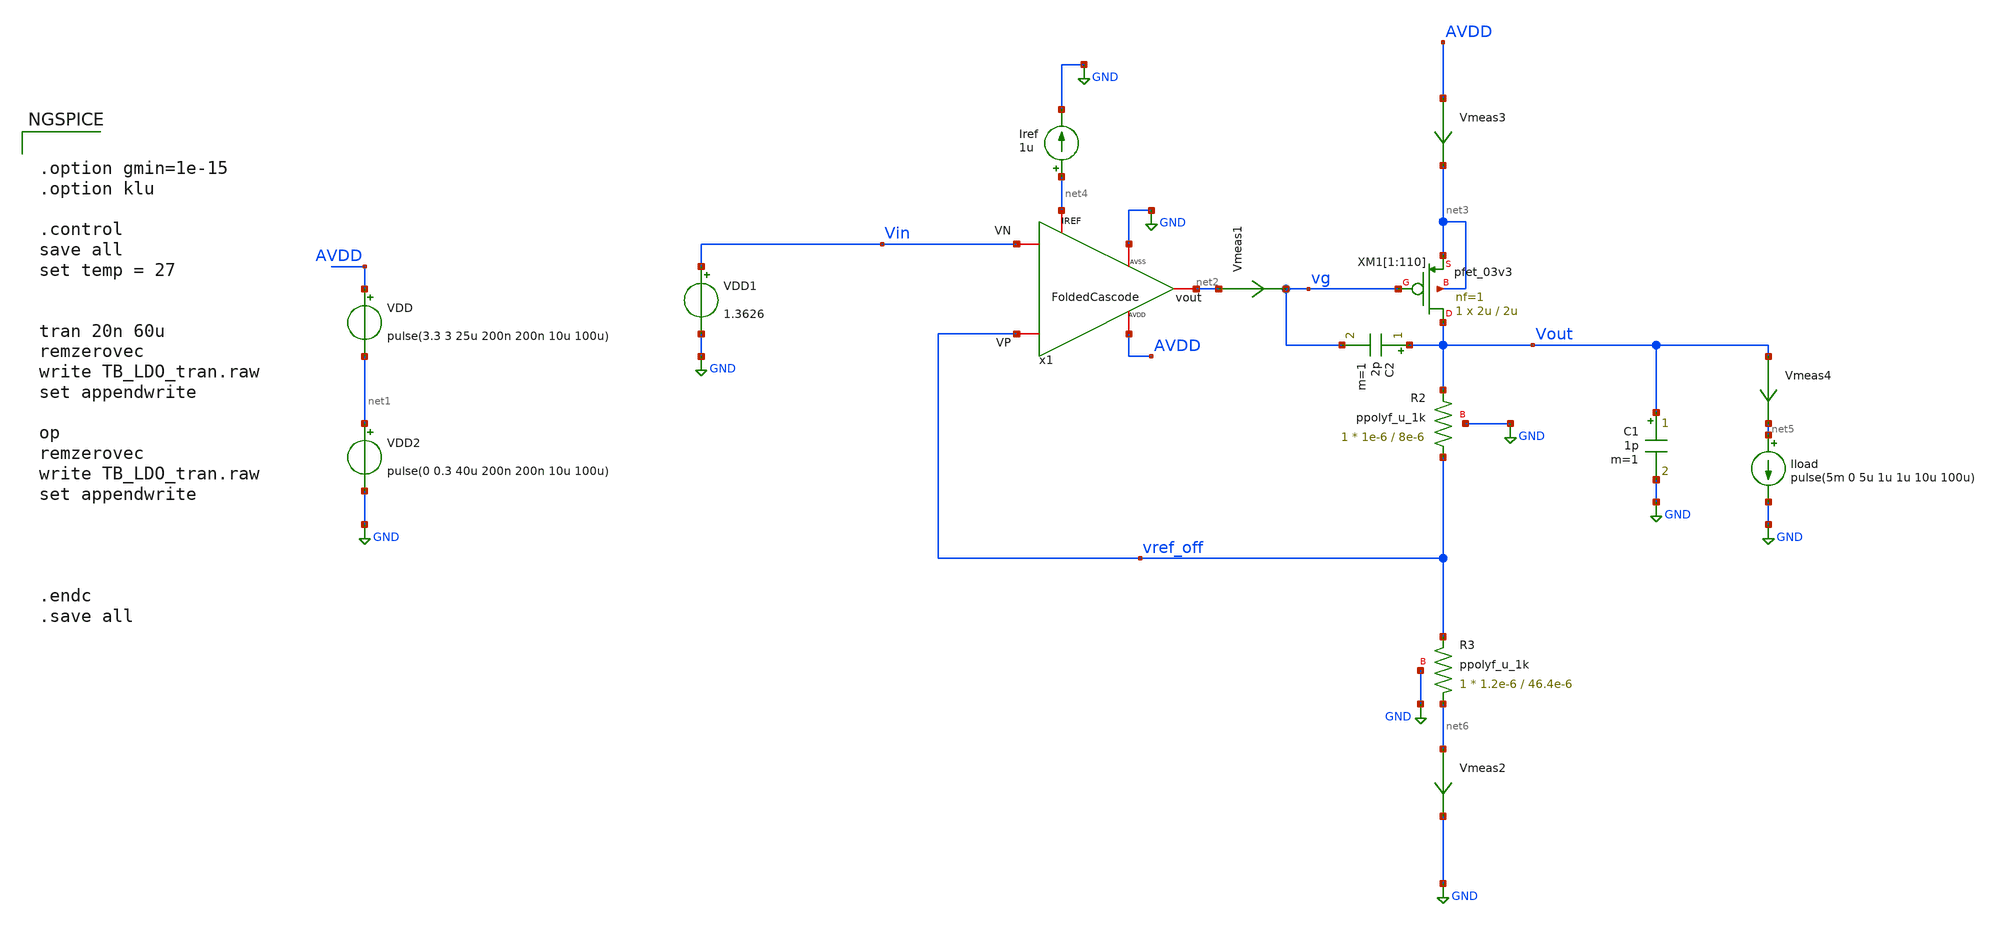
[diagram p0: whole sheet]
** sch_path: Voltage_Reference/LDO/TB_LDO_tran.sch
**.subckt TB_LDO_tran
VDD AVDD net1 pulse(3.3 3 25u 200n 200n 10u 100u)
Iref net4 GND 1u
Vmeas2 net6 GND 0
.save i(vmeas2)
XM1[1] Vout vg net3 net3 pfet_03v3 L=2u W=2u nf=1 ad='int((nf+1)/2) * W/nf * 0.18u' as='int((nf+2)/2) * W/nf * 0.18u'
+ pd='2*int((nf+1)/2) * (W/nf + 0.18u)' ps='2*int((nf+2)/2) * (W/nf + 0.18u)' nrd='0.18u / W' nrs='0.18u / W'
+ sa=0 sb=0 sd=0 m=1
XM1[2] Vout vg net3 net3 pfet_03v3 L=2u W=2u nf=1 ad='int((nf+1)/2) * W/nf * 0.18u' as='int((nf+2)/2) * W/nf * 0.18u'
+ pd='2*int((nf+1)/2) * (W/nf + 0.18u)' ps='2*int((nf+2)/2) * (W/nf + 0.18u)' nrd='0.18u / W' nrs='0.18u / W'
+ sa=0 sb=0 sd=0 m=1
XM1[3] Vout vg net3 net3 pfet_03v3 L=2u W=2u nf=1 ad='int((nf+1)/2) * W/nf * 0.18u' as='int((nf+2)/2) * W/nf * 0.18u'
+ pd='2*int((nf+1)/2) * (W/nf + 0.18u)' ps='2*int((nf+2)/2) * (W/nf + 0.18u)' nrd='0.18u / W' nrs='0.18u / W'
+ sa=0 sb=0 sd=0 m=1
XM1[4] Vout vg net3 net3 pfet_03v3 L=2u W=2u nf=1 ad='int((nf+1)/2) * W/nf * 0.18u' as='int((nf+2)/2) * W/nf * 0.18u'
+ pd='2*int((nf+1)/2) * (W/nf + 0.18u)' ps='2*int((nf+2)/2) * (W/nf + 0.18u)' nrd='0.18u / W' nrs='0.18u / W'
+ sa=0 sb=0 sd=0 m=1
XM1[5] Vout vg net3 net3 pfet_03v3 L=2u W=2u nf=1 ad='int((nf+1)/2) * W/nf * 0.18u' as='int((nf+2)/2) * W/nf * 0.18u'
+ pd='2*int((nf+1)/2) * (W/nf + 0.18u)' ps='2*int((nf+2)/2) * (W/nf + 0.18u)' nrd='0.18u / W' nrs='0.18u / W'
+ sa=0 sb=0 sd=0 m=1
XM1[6] Vout vg net3 net3 pfet_03v3 L=2u W=2u nf=1 ad='int((nf+1)/2) * W/nf * 0.18u' as='int((nf+2)/2) * W/nf * 0.18u'
+ pd='2*int((nf+1)/2) * (W/nf + 0.18u)' ps='2*int((nf+2)/2) * (W/nf + 0.18u)' nrd='0.18u / W' nrs='0.18u / W'
+ sa=0 sb=0 sd=0 m=1
XM1[7] Vout vg net3 net3 pfet_03v3 L=2u W=2u nf=1 ad='int((nf+1)/2) * W/nf * 0.18u' as='int((nf+2)/2) * W/nf * 0.18u'
+ pd='2*int((nf+1)/2) * (W/nf + 0.18u)' ps='2*int((nf+2)/2) * (W/nf + 0.18u)' nrd='0.18u / W' nrs='0.18u / W'
+ sa=0 sb=0 sd=0 m=1
XM1[8] Vout vg net3 net3 pfet_03v3 L=2u W=2u nf=1 ad='int((nf+1)/2) * W/nf * 0.18u' as='int((nf+2)/2) * W/nf * 0.18u'
+ pd='2*int((nf+1)/2) * (W/nf + 0.18u)' ps='2*int((nf+2)/2) * (W/nf + 0.18u)' nrd='0.18u / W' nrs='0.18u / W'
+ sa=0 sb=0 sd=0 m=1
XM1[9] Vout vg net3 net3 pfet_03v3 L=2u W=2u nf=1 ad='int((nf+1)/2) * W/nf * 0.18u' as='int((nf+2)/2) * W/nf * 0.18u'
+ pd='2*int((nf+1)/2) * (W/nf + 0.18u)' ps='2*int((nf+2)/2) * (W/nf + 0.18u)' nrd='0.18u / W' nrs='0.18u / W'
+ sa=0 sb=0 sd=0 m=1
XM1[10] Vout vg net3 net3 pfet_03v3 L=2u W=2u nf=1 ad='int((nf+1)/2) * W/nf * 0.18u' as='int((nf+2)/2) * W/nf * 0.18u'
+ pd='2*int((nf+1)/2) * (W/nf + 0.18u)' ps='2*int((nf+2)/2) * (W/nf + 0.18u)' nrd='0.18u / W' nrs='0.18u / W'
+ sa=0 sb=0 sd=0 m=1
XM1[11] Vout vg net3 net3 pfet_03v3 L=2u W=2u nf=1 ad='int((nf+1)/2) * W/nf * 0.18u' as='int((nf+2)/2) * W/nf * 0.18u'
+ pd='2*int((nf+1)/2) * (W/nf + 0.18u)' ps='2*int((nf+2)/2) * (W/nf + 0.18u)' nrd='0.18u / W' nrs='0.18u / W'
+ sa=0 sb=0 sd=0 m=1
XM1[12] Vout vg net3 net3 pfet_03v3 L=2u W=2u nf=1 ad='int((nf+1)/2) * W/nf * 0.18u' as='int((nf+2)/2) * W/nf * 0.18u'
+ pd='2*int((nf+1)/2) * (W/nf + 0.18u)' ps='2*int((nf+2)/2) * (W/nf + 0.18u)' nrd='0.18u / W' nrs='0.18u / W'
+ sa=0 sb=0 sd=0 m=1
XM1[13] Vout vg net3 net3 pfet_03v3 L=2u W=2u nf=1 ad='int((nf+1)/2) * W/nf * 0.18u' as='int((nf+2)/2) * W/nf * 0.18u'
+ pd='2*int((nf+1)/2) * (W/nf + 0.18u)' ps='2*int((nf+2)/2) * (W/nf + 0.18u)' nrd='0.18u / W' nrs='0.18u / W'
+ sa=0 sb=0 sd=0 m=1
XM1[14] Vout vg net3 net3 pfet_03v3 L=2u W=2u nf=1 ad='int((nf+1)/2) * W/nf * 0.18u' as='int((nf+2)/2) * W/nf * 0.18u'
+ pd='2*int((nf+1)/2) * (W/nf + 0.18u)' ps='2*int((nf+2)/2) * (W/nf + 0.18u)' nrd='0.18u / W' nrs='0.18u / W'
+ sa=0 sb=0 sd=0 m=1
XM1[15] Vout vg net3 net3 pfet_03v3 L=2u W=2u nf=1 ad='int((nf+1)/2) * W/nf * 0.18u' as='int((nf+2)/2) * W/nf * 0.18u'
+ pd='2*int((nf+1)/2) * (W/nf + 0.18u)' ps='2*int((nf+2)/2) * (W/nf + 0.18u)' nrd='0.18u / W' nrs='0.18u / W'
+ sa=0 sb=0 sd=0 m=1
XM1[16] Vout vg net3 net3 pfet_03v3 L=2u W=2u nf=1 ad='int((nf+1)/2) * W/nf * 0.18u' as='int((nf+2)/2) * W/nf * 0.18u'
+ pd='2*int((nf+1)/2) * (W/nf + 0.18u)' ps='2*int((nf+2)/2) * (W/nf + 0.18u)' nrd='0.18u / W' nrs='0.18u / W'
+ sa=0 sb=0 sd=0 m=1
XM1[17] Vout vg net3 net3 pfet_03v3 L=2u W=2u nf=1 ad='int((nf+1)/2) * W/nf * 0.18u' as='int((nf+2)/2) * W/nf * 0.18u'
+ pd='2*int((nf+1)/2) * (W/nf + 0.18u)' ps='2*int((nf+2)/2) * (W/nf + 0.18u)' nrd='0.18u / W' nrs='0.18u / W'
+ sa=0 sb=0 sd=0 m=1
XM1[18] Vout vg net3 net3 pfet_03v3 L=2u W=2u nf=1 ad='int((nf+1)/2) * W/nf * 0.18u' as='int((nf+2)/2) * W/nf * 0.18u'
+ pd='2*int((nf+1)/2) * (W/nf + 0.18u)' ps='2*int((nf+2)/2) * (W/nf + 0.18u)' nrd='0.18u / W' nrs='0.18u / W'
+ sa=0 sb=0 sd=0 m=1
XM1[19] Vout vg net3 net3 pfet_03v3 L=2u W=2u nf=1 ad='int((nf+1)/2) * W/nf * 0.18u' as='int((nf+2)/2) * W/nf * 0.18u'
+ pd='2*int((nf+1)/2) * (W/nf + 0.18u)' ps='2*int((nf+2)/2) * (W/nf + 0.18u)' nrd='0.18u / W' nrs='0.18u / W'
+ sa=0 sb=0 sd=0 m=1
XM1[20] Vout vg net3 net3 pfet_03v3 L=2u W=2u nf=1 ad='int((nf+1)/2) * W/nf * 0.18u' as='int((nf+2)/2) * W/nf * 0.18u'
+ pd='2*int((nf+1)/2) * (W/nf + 0.18u)' ps='2*int((nf+2)/2) * (W/nf + 0.18u)' nrd='0.18u / W' nrs='0.18u / W'
+ sa=0 sb=0 sd=0 m=1
XM1[21] Vout vg net3 net3 pfet_03v3 L=2u W=2u nf=1 ad='int((nf+1)/2) * W/nf * 0.18u' as='int((nf+2)/2) * W/nf * 0.18u'
+ pd='2*int((nf+1)/2) * (W/nf + 0.18u)' ps='2*int((nf+2)/2) * (W/nf + 0.18u)' nrd='0.18u / W' nrs='0.18u / W'
+ sa=0 sb=0 sd=0 m=1
XM1[22] Vout vg net3 net3 pfet_03v3 L=2u W=2u nf=1 ad='int((nf+1)/2) * W/nf * 0.18u' as='int((nf+2)/2) * W/nf * 0.18u'
+ pd='2*int((nf+1)/2) * (W/nf + 0.18u)' ps='2*int((nf+2)/2) * (W/nf + 0.18u)' nrd='0.18u / W' nrs='0.18u / W'
+ sa=0 sb=0 sd=0 m=1
XM1[23] Vout vg net3 net3 pfet_03v3 L=2u W=2u nf=1 ad='int((nf+1)/2) * W/nf * 0.18u' as='int((nf+2)/2) * W/nf * 0.18u'
+ pd='2*int((nf+1)/2) * (W/nf + 0.18u)' ps='2*int((nf+2)/2) * (W/nf + 0.18u)' nrd='0.18u / W' nrs='0.18u / W'
+ sa=0 sb=0 sd=0 m=1
XM1[24] Vout vg net3 net3 pfet_03v3 L=2u W=2u nf=1 ad='int((nf+1)/2) * W/nf * 0.18u' as='int((nf+2)/2) * W/nf * 0.18u'
+ pd='2*int((nf+1)/2) * (W/nf + 0.18u)' ps='2*int((nf+2)/2) * (W/nf + 0.18u)' nrd='0.18u / W' nrs='0.18u / W'
+ sa=0 sb=0 sd=0 m=1
XM1[25] Vout vg net3 net3 pfet_03v3 L=2u W=2u nf=1 ad='int((nf+1)/2) * W/nf * 0.18u' as='int((nf+2)/2) * W/nf * 0.18u'
+ pd='2*int((nf+1)/2) * (W/nf + 0.18u)' ps='2*int((nf+2)/2) * (W/nf + 0.18u)' nrd='0.18u / W' nrs='0.18u / W'
+ sa=0 sb=0 sd=0 m=1
XM1[26] Vout vg net3 net3 pfet_03v3 L=2u W=2u nf=1 ad='int((nf+1)/2) * W/nf * 0.18u' as='int((nf+2)/2) * W/nf * 0.18u'
+ pd='2*int((nf+1)/2) * (W/nf + 0.18u)' ps='2*int((nf+2)/2) * (W/nf + 0.18u)' nrd='0.18u / W' nrs='0.18u / W'
+ sa=0 sb=0 sd=0 m=1
XM1[27] Vout vg net3 net3 pfet_03v3 L=2u W=2u nf=1 ad='int((nf+1)/2) * W/nf * 0.18u' as='int((nf+2)/2) * W/nf * 0.18u'
+ pd='2*int((nf+1)/2) * (W/nf + 0.18u)' ps='2*int((nf+2)/2) * (W/nf + 0.18u)' nrd='0.18u / W' nrs='0.18u / W'
+ sa=0 sb=0 sd=0 m=1
XM1[28] Vout vg net3 net3 pfet_03v3 L=2u W=2u nf=1 ad='int((nf+1)/2) * W/nf * 0.18u' as='int((nf+2)/2) * W/nf * 0.18u'
+ pd='2*int((nf+1)/2) * (W/nf + 0.18u)' ps='2*int((nf+2)/2) * (W/nf + 0.18u)' nrd='0.18u / W' nrs='0.18u / W'
+ sa=0 sb=0 sd=0 m=1
XM1[29] Vout vg net3 net3 pfet_03v3 L=2u W=2u nf=1 ad='int((nf+1)/2) * W/nf * 0.18u' as='int((nf+2)/2) * W/nf * 0.18u'
+ pd='2*int((nf+1)/2) * (W/nf + 0.18u)' ps='2*int((nf+2)/2) * (W/nf + 0.18u)' nrd='0.18u / W' nrs='0.18u / W'
+ sa=0 sb=0 sd=0 m=1
XM1[30] Vout vg net3 net3 pfet_03v3 L=2u W=2u nf=1 ad='int((nf+1)/2) * W/nf * 0.18u' as='int((nf+2)/2) * W/nf * 0.18u'
+ pd='2*int((nf+1)/2) * (W/nf + 0.18u)' ps='2*int((nf+2)/2) * (W/nf + 0.18u)' nrd='0.18u / W' nrs='0.18u / W'
+ sa=0 sb=0 sd=0 m=1
XM1[31] Vout vg net3 net3 pfet_03v3 L=2u W=2u nf=1 ad='int((nf+1)/2) * W/nf * 0.18u' as='int((nf+2)/2) * W/nf * 0.18u'
+ pd='2*int((nf+1)/2) * (W/nf + 0.18u)' ps='2*int((nf+2)/2) * (W/nf + 0.18u)' nrd='0.18u / W' nrs='0.18u / W'
+ sa=0 sb=0 sd=0 m=1
XM1[32] Vout vg net3 net3 pfet_03v3 L=2u W=2u nf=1 ad='int((nf+1)/2) * W/nf * 0.18u' as='int((nf+2)/2) * W/nf * 0.18u'
+ pd='2*int((nf+1)/2) * (W/nf + 0.18u)' ps='2*int((nf+2)/2) * (W/nf + 0.18u)' nrd='0.18u / W' nrs='0.18u / W'
+ sa=0 sb=0 sd=0 m=1
XM1[33] Vout vg net3 net3 pfet_03v3 L=2u W=2u nf=1 ad='int((nf+1)/2) * W/nf * 0.18u' as='int((nf+2)/2) * W/nf * 0.18u'
+ pd='2*int((nf+1)/2) * (W/nf + 0.18u)' ps='2*int((nf+2)/2) * (W/nf + 0.18u)' nrd='0.18u / W' nrs='0.18u / W'
+ sa=0 sb=0 sd=0 m=1
XM1[34] Vout vg net3 net3 pfet_03v3 L=2u W=2u nf=1 ad='int((nf+1)/2) * W/nf * 0.18u' as='int((nf+2)/2) * W/nf * 0.18u'
+ pd='2*int((nf+1)/2) * (W/nf + 0.18u)' ps='2*int((nf+2)/2) * (W/nf + 0.18u)' nrd='0.18u / W' nrs='0.18u / W'
+ sa=0 sb=0 sd=0 m=1
XM1[35] Vout vg net3 net3 pfet_03v3 L=2u W=2u nf=1 ad='int((nf+1)/2) * W/nf * 0.18u' as='int((nf+2)/2) * W/nf * 0.18u'
+ pd='2*int((nf+1)/2) * (W/nf + 0.18u)' ps='2*int((nf+2)/2) * (W/nf + 0.18u)' nrd='0.18u / W' nrs='0.18u / W'
+ sa=0 sb=0 sd=0 m=1
XM1[36] Vout vg net3 net3 pfet_03v3 L=2u W=2u nf=1 ad='int((nf+1)/2) * W/nf * 0.18u' as='int((nf+2)/2) * W/nf * 0.18u'
+ pd='2*int((nf+1)/2) * (W/nf + 0.18u)' ps='2*int((nf+2)/2) * (W/nf + 0.18u)' nrd='0.18u / W' nrs='0.18u / W'
+ sa=0 sb=0 sd=0 m=1
XM1[37] Vout vg net3 net3 pfet_03v3 L=2u W=2u nf=1 ad='int((nf+1)/2) * W/nf * 0.18u' as='int((nf+2)/2) * W/nf * 0.18u'
+ pd='2*int((nf+1)/2) * (W/nf + 0.18u)' ps='2*int((nf+2)/2) * (W/nf + 0.18u)' nrd='0.18u / W' nrs='0.18u / W'
+ sa=0 sb=0 sd=0 m=1
XM1[38] Vout vg net3 net3 pfet_03v3 L=2u W=2u nf=1 ad='int((nf+1)/2) * W/nf * 0.18u' as='int((nf+2)/2) * W/nf * 0.18u'
+ pd='2*int((nf+1)/2) * (W/nf + 0.18u)' ps='2*int((nf+2)/2) * (W/nf + 0.18u)' nrd='0.18u / W' nrs='0.18u / W'
+ sa=0 sb=0 sd=0 m=1
XM1[39] Vout vg net3 net3 pfet_03v3 L=2u W=2u nf=1 ad='int((nf+1)/2) * W/nf * 0.18u' as='int((nf+2)/2) * W/nf * 0.18u'
+ pd='2*int((nf+1)/2) * (W/nf + 0.18u)' ps='2*int((nf+2)/2) * (W/nf + 0.18u)' nrd='0.18u / W' nrs='0.18u / W'
+ sa=0 sb=0 sd=0 m=1
XM1[40] Vout vg net3 net3 pfet_03v3 L=2u W=2u nf=1 ad='int((nf+1)/2) * W/nf * 0.18u' as='int((nf+2)/2) * W/nf * 0.18u'
+ pd='2*int((nf+1)/2) * (W/nf + 0.18u)' ps='2*int((nf+2)/2) * (W/nf + 0.18u)' nrd='0.18u / W' nrs='0.18u / W'
+ sa=0 sb=0 sd=0 m=1
XM1[41] Vout vg net3 net3 pfet_03v3 L=2u W=2u nf=1 ad='int((nf+1)/2) * W/nf * 0.18u' as='int((nf+2)/2) * W/nf * 0.18u'
+ pd='2*int((nf+1)/2) * (W/nf + 0.18u)' ps='2*int((nf+2)/2) * (W/nf + 0.18u)' nrd='0.18u / W' nrs='0.18u / W'
+ sa=0 sb=0 sd=0 m=1
XM1[42] Vout vg net3 net3 pfet_03v3 L=2u W=2u nf=1 ad='int((nf+1)/2) * W/nf * 0.18u' as='int((nf+2)/2) * W/nf * 0.18u'
+ pd='2*int((nf+1)/2) * (W/nf + 0.18u)' ps='2*int((nf+2)/2) * (W/nf + 0.18u)' nrd='0.18u / W' nrs='0.18u / W'
+ sa=0 sb=0 sd=0 m=1
XM1[43] Vout vg net3 net3 pfet_03v3 L=2u W=2u nf=1 ad='int((nf+1)/2) * W/nf * 0.18u' as='int((nf+2)/2) * W/nf * 0.18u'
+ pd='2*int((nf+1)/2) * (W/nf + 0.18u)' ps='2*int((nf+2)/2) * (W/nf + 0.18u)' nrd='0.18u / W' nrs='0.18u / W'
+ sa=0 sb=0 sd=0 m=1
XM1[44] Vout vg net3 net3 pfet_03v3 L=2u W=2u nf=1 ad='int((nf+1)/2) * W/nf * 0.18u' as='int((nf+2)/2) * W/nf * 0.18u'
+ pd='2*int((nf+1)/2) * (W/nf + 0.18u)' ps='2*int((nf+2)/2) * (W/nf + 0.18u)' nrd='0.18u / W' nrs='0.18u / W'
+ sa=0 sb=0 sd=0 m=1
XM1[45] Vout vg net3 net3 pfet_03v3 L=2u W=2u nf=1 ad='int((nf+1)/2) * W/nf * 0.18u' as='int((nf+2)/2) * W/nf * 0.18u'
+ pd='2*int((nf+1)/2) * (W/nf + 0.18u)' ps='2*int((nf+2)/2) * (W/nf + 0.18u)' nrd='0.18u / W' nrs='0.18u / W'
+ sa=0 sb=0 sd=0 m=1
XM1[46] Vout vg net3 net3 pfet_03v3 L=2u W=2u nf=1 ad='int((nf+1)/2) * W/nf * 0.18u' as='int((nf+2)/2) * W/nf * 0.18u'
+ pd='2*int((nf+1)/2) * (W/nf + 0.18u)' ps='2*int((nf+2)/2) * (W/nf + 0.18u)' nrd='0.18u / W' nrs='0.18u / W'
+ sa=0 sb=0 sd=0 m=1
XM1[47] Vout vg net3 net3 pfet_03v3 L=2u W=2u nf=1 ad='int((nf+1)/2) * W/nf * 0.18u' as='int((nf+2)/2) * W/nf * 0.18u'
+ pd='2*int((nf+1)/2) * (W/nf + 0.18u)' ps='2*int((nf+2)/2) * (W/nf + 0.18u)' nrd='0.18u / W' nrs='0.18u / W'
+ sa=0 sb=0 sd=0 m=1
XM1[48] Vout vg net3 net3 pfet_03v3 L=2u W=2u nf=1 ad='int((nf+1)/2) * W/nf * 0.18u' as='int((nf+2)/2) * W/nf * 0.18u'
+ pd='2*int((nf+1)/2) * (W/nf + 0.18u)' ps='2*int((nf+2)/2) * (W/nf + 0.18u)' nrd='0.18u / W' nrs='0.18u / W'
+ sa=0 sb=0 sd=0 m=1
XM1[49] Vout vg net3 net3 pfet_03v3 L=2u W=2u nf=1 ad='int((nf+1)/2) * W/nf * 0.18u' as='int((nf+2)/2) * W/nf * 0.18u'
+ pd='2*int((nf+1)/2) * (W/nf + 0.18u)' ps='2*int((nf+2)/2) * (W/nf + 0.18u)' nrd='0.18u / W' nrs='0.18u / W'
+ sa=0 sb=0 sd=0 m=1
XM1[50] Vout vg net3 net3 pfet_03v3 L=2u W=2u nf=1 ad='int((nf+1)/2) * W/nf * 0.18u' as='int((nf+2)/2) * W/nf * 0.18u'
+ pd='2*int((nf+1)/2) * (W/nf + 0.18u)' ps='2*int((nf+2)/2) * (W/nf + 0.18u)' nrd='0.18u / W' nrs='0.18u / W'
+ sa=0 sb=0 sd=0 m=1
XM1[51] Vout vg net3 net3 pfet_03v3 L=2u W=2u nf=1 ad='int((nf+1)/2) * W/nf * 0.18u' as='int((nf+2)/2) * W/nf * 0.18u'
+ pd='2*int((nf+1)/2) * (W/nf + 0.18u)' ps='2*int((nf+2)/2) * (W/nf + 0.18u)' nrd='0.18u / W' nrs='0.18u / W'
+ sa=0 sb=0 sd=0 m=1
XM1[52] Vout vg net3 net3 pfet_03v3 L=2u W=2u nf=1 ad='int((nf+1)/2) * W/nf * 0.18u' as='int((nf+2)/2) * W/nf * 0.18u'
+ pd='2*int((nf+1)/2) * (W/nf + 0.18u)' ps='2*int((nf+2)/2) * (W/nf + 0.18u)' nrd='0.18u / W' nrs='0.18u / W'
+ sa=0 sb=0 sd=0 m=1
XM1[53] Vout vg net3 net3 pfet_03v3 L=2u W=2u nf=1 ad='int((nf+1)/2) * W/nf * 0.18u' as='int((nf+2)/2) * W/nf * 0.18u'
+ pd='2*int((nf+1)/2) * (W/nf + 0.18u)' ps='2*int((nf+2)/2) * (W/nf + 0.18u)' nrd='0.18u / W' nrs='0.18u / W'
+ sa=0 sb=0 sd=0 m=1
XM1[54] Vout vg net3 net3 pfet_03v3 L=2u W=2u nf=1 ad='int((nf+1)/2) * W/nf * 0.18u' as='int((nf+2)/2) * W/nf * 0.18u'
+ pd='2*int((nf+1)/2) * (W/nf + 0.18u)' ps='2*int((nf+2)/2) * (W/nf + 0.18u)' nrd='0.18u / W' nrs='0.18u / W'
+ sa=0 sb=0 sd=0 m=1
XM1[55] Vout vg net3 net3 pfet_03v3 L=2u W=2u nf=1 ad='int((nf+1)/2) * W/nf * 0.18u' as='int((nf+2)/2) * W/nf * 0.18u'
+ pd='2*int((nf+1)/2) * (W/nf + 0.18u)' ps='2*int((nf+2)/2) * (W/nf + 0.18u)' nrd='0.18u / W' nrs='0.18u / W'
+ sa=0 sb=0 sd=0 m=1
XM1[56] Vout vg net3 net3 pfet_03v3 L=2u W=2u nf=1 ad='int((nf+1)/2) * W/nf * 0.18u' as='int((nf+2)/2) * W/nf * 0.18u'
+ pd='2*int((nf+1)/2) * (W/nf + 0.18u)' ps='2*int((nf+2)/2) * (W/nf + 0.18u)' nrd='0.18u / W' nrs='0.18u / W'
+ sa=0 sb=0 sd=0 m=1
XM1[57] Vout vg net3 net3 pfet_03v3 L=2u W=2u nf=1 ad='int((nf+1)/2) * W/nf * 0.18u' as='int((nf+2)/2) * W/nf * 0.18u'
+ pd='2*int((nf+1)/2) * (W/nf + 0.18u)' ps='2*int((nf+2)/2) * (W/nf + 0.18u)' nrd='0.18u / W' nrs='0.18u / W'
+ sa=0 sb=0 sd=0 m=1
XM1[58] Vout vg net3 net3 pfet_03v3 L=2u W=2u nf=1 ad='int((nf+1)/2) * W/nf * 0.18u' as='int((nf+2)/2) * W/nf * 0.18u'
+ pd='2*int((nf+1)/2) * (W/nf + 0.18u)' ps='2*int((nf+2)/2) * (W/nf + 0.18u)' nrd='0.18u / W' nrs='0.18u / W'
+ sa=0 sb=0 sd=0 m=1
XM1[59] Vout vg net3 net3 pfet_03v3 L=2u W=2u nf=1 ad='int((nf+1)/2) * W/nf * 0.18u' as='int((nf+2)/2) * W/nf * 0.18u'
+ pd='2*int((nf+1)/2) * (W/nf + 0.18u)' ps='2*int((nf+2)/2) * (W/nf + 0.18u)' nrd='0.18u / W' nrs='0.18u / W'
+ sa=0 sb=0 sd=0 m=1
XM1[60] Vout vg net3 net3 pfet_03v3 L=2u W=2u nf=1 ad='int((nf+1)/2) * W/nf * 0.18u' as='int((nf+2)/2) * W/nf * 0.18u'
+ pd='2*int((nf+1)/2) * (W/nf + 0.18u)' ps='2*int((nf+2)/2) * (W/nf + 0.18u)' nrd='0.18u / W' nrs='0.18u / W'
+ sa=0 sb=0 sd=0 m=1
XM1[61] Vout vg net3 net3 pfet_03v3 L=2u W=2u nf=1 ad='int((nf+1)/2) * W/nf * 0.18u' as='int((nf+2)/2) * W/nf * 0.18u'
+ pd='2*int((nf+1)/2) * (W/nf + 0.18u)' ps='2*int((nf+2)/2) * (W/nf + 0.18u)' nrd='0.18u / W' nrs='0.18u / W'
+ sa=0 sb=0 sd=0 m=1
XM1[62] Vout vg net3 net3 pfet_03v3 L=2u W=2u nf=1 ad='int((nf+1)/2) * W/nf * 0.18u' as='int((nf+2)/2) * W/nf * 0.18u'
+ pd='2*int((nf+1)/2) * (W/nf + 0.18u)' ps='2*int((nf+2)/2) * (W/nf + 0.18u)' nrd='0.18u / W' nrs='0.18u / W'
+ sa=0 sb=0 sd=0 m=1
XM1[63] Vout vg net3 net3 pfet_03v3 L=2u W=2u nf=1 ad='int((nf+1)/2) * W/nf * 0.18u' as='int((nf+2)/2) * W/nf * 0.18u'
+ pd='2*int((nf+1)/2) * (W/nf + 0.18u)' ps='2*int((nf+2)/2) * (W/nf + 0.18u)' nrd='0.18u / W' nrs='0.18u / W'
+ sa=0 sb=0 sd=0 m=1
XM1[64] Vout vg net3 net3 pfet_03v3 L=2u W=2u nf=1 ad='int((nf+1)/2) * W/nf * 0.18u' as='int((nf+2)/2) * W/nf * 0.18u'
+ pd='2*int((nf+1)/2) * (W/nf + 0.18u)' ps='2*int((nf+2)/2) * (W/nf + 0.18u)' nrd='0.18u / W' nrs='0.18u / W'
+ sa=0 sb=0 sd=0 m=1
XM1[65] Vout vg net3 net3 pfet_03v3 L=2u W=2u nf=1 ad='int((nf+1)/2) * W/nf * 0.18u' as='int((nf+2)/2) * W/nf * 0.18u'
+ pd='2*int((nf+1)/2) * (W/nf + 0.18u)' ps='2*int((nf+2)/2) * (W/nf + 0.18u)' nrd='0.18u / W' nrs='0.18u / W'
+ sa=0 sb=0 sd=0 m=1
XM1[66] Vout vg net3 net3 pfet_03v3 L=2u W=2u nf=1 ad='int((nf+1)/2) * W/nf * 0.18u' as='int((nf+2)/2) * W/nf * 0.18u'
+ pd='2*int((nf+1)/2) * (W/nf + 0.18u)' ps='2*int((nf+2)/2) * (W/nf + 0.18u)' nrd='0.18u / W' nrs='0.18u / W'
+ sa=0 sb=0 sd=0 m=1
XM1[67] Vout vg net3 net3 pfet_03v3 L=2u W=2u nf=1 ad='int((nf+1)/2) * W/nf * 0.18u' as='int((nf+2)/2) * W/nf * 0.18u'
+ pd='2*int((nf+1)/2) * (W/nf + 0.18u)' ps='2*int((nf+2)/2) * (W/nf + 0.18u)' nrd='0.18u / W' nrs='0.18u / W'
+ sa=0 sb=0 sd=0 m=1
XM1[68] Vout vg net3 net3 pfet_03v3 L=2u W=2u nf=1 ad='int((nf+1)/2) * W/nf * 0.18u' as='int((nf+2)/2) * W/nf * 0.18u'
+ pd='2*int((nf+1)/2) * (W/nf + 0.18u)' ps='2*int((nf+2)/2) * (W/nf + 0.18u)' nrd='0.18u / W' nrs='0.18u / W'
+ sa=0 sb=0 sd=0 m=1
XM1[69] Vout vg net3 net3 pfet_03v3 L=2u W=2u nf=1 ad='int((nf+1)/2) * W/nf * 0.18u' as='int((nf+2)/2) * W/nf * 0.18u'
+ pd='2*int((nf+1)/2) * (W/nf + 0.18u)' ps='2*int((nf+2)/2) * (W/nf + 0.18u)' nrd='0.18u / W' nrs='0.18u / W'
+ sa=0 sb=0 sd=0 m=1
XM1[70] Vout vg net3 net3 pfet_03v3 L=2u W=2u nf=1 ad='int((nf+1)/2) * W/nf * 0.18u' as='int((nf+2)/2) * W/nf * 0.18u'
+ pd='2*int((nf+1)/2) * (W/nf + 0.18u)' ps='2*int((nf+2)/2) * (W/nf + 0.18u)' nrd='0.18u / W' nrs='0.18u / W'
+ sa=0 sb=0 sd=0 m=1
XM1[71] Vout vg net3 net3 pfet_03v3 L=2u W=2u nf=1 ad='int((nf+1)/2) * W/nf * 0.18u' as='int((nf+2)/2) * W/nf * 0.18u'
+ pd='2*int((nf+1)/2) * (W/nf + 0.18u)' ps='2*int((nf+2)/2) * (W/nf + 0.18u)' nrd='0.18u / W' nrs='0.18u / W'
+ sa=0 sb=0 sd=0 m=1
XM1[72] Vout vg net3 net3 pfet_03v3 L=2u W=2u nf=1 ad='int((nf+1)/2) * W/nf * 0.18u' as='int((nf+2)/2) * W/nf * 0.18u'
+ pd='2*int((nf+1)/2) * (W/nf + 0.18u)' ps='2*int((nf+2)/2) * (W/nf + 0.18u)' nrd='0.18u / W' nrs='0.18u / W'
+ sa=0 sb=0 sd=0 m=1
XM1[73] Vout vg net3 net3 pfet_03v3 L=2u W=2u nf=1 ad='int((nf+1)/2) * W/nf * 0.18u' as='int((nf+2)/2) * W/nf * 0.18u'
+ pd='2*int((nf+1)/2) * (W/nf + 0.18u)' ps='2*int((nf+2)/2) * (W/nf + 0.18u)' nrd='0.18u / W' nrs='0.18u / W'
+ sa=0 sb=0 sd=0 m=1
XM1[74] Vout vg net3 net3 pfet_03v3 L=2u W=2u nf=1 ad='int((nf+1)/2) * W/nf * 0.18u' as='int((nf+2)/2) * W/nf * 0.18u'
+ pd='2*int((nf+1)/2) * (W/nf + 0.18u)' ps='2*int((nf+2)/2) * (W/nf + 0.18u)' nrd='0.18u / W' nrs='0.18u / W'
+ sa=0 sb=0 sd=0 m=1
XM1[75] Vout vg net3 net3 pfet_03v3 L=2u W=2u nf=1 ad='int((nf+1)/2) * W/nf * 0.18u' as='int((nf+2)/2) * W/nf * 0.18u'
+ pd='2*int((nf+1)/2) * (W/nf + 0.18u)' ps='2*int((nf+2)/2) * (W/nf + 0.18u)' nrd='0.18u / W' nrs='0.18u / W'
+ sa=0 sb=0 sd=0 m=1
XM1[76] Vout vg net3 net3 pfet_03v3 L=2u W=2u nf=1 ad='int((nf+1)/2) * W/nf * 0.18u' as='int((nf+2)/2) * W/nf * 0.18u'
+ pd='2*int((nf+1)/2) * (W/nf + 0.18u)' ps='2*int((nf+2)/2) * (W/nf + 0.18u)' nrd='0.18u / W' nrs='0.18u / W'
+ sa=0 sb=0 sd=0 m=1
XM1[77] Vout vg net3 net3 pfet_03v3 L=2u W=2u nf=1 ad='int((nf+1)/2) * W/nf * 0.18u' as='int((nf+2)/2) * W/nf * 0.18u'
+ pd='2*int((nf+1)/2) * (W/nf + 0.18u)' ps='2*int((nf+2)/2) * (W/nf + 0.18u)' nrd='0.18u / W' nrs='0.18u / W'
+ sa=0 sb=0 sd=0 m=1
XM1[78] Vout vg net3 net3 pfet_03v3 L=2u W=2u nf=1 ad='int((nf+1)/2) * W/nf * 0.18u' as='int((nf+2)/2) * W/nf * 0.18u'
+ pd='2*int((nf+1)/2) * (W/nf + 0.18u)' ps='2*int((nf+2)/2) * (W/nf + 0.18u)' nrd='0.18u / W' nrs='0.18u / W'
+ sa=0 sb=0 sd=0 m=1
XM1[79] Vout vg net3 net3 pfet_03v3 L=2u W=2u nf=1 ad='int((nf+1)/2) * W/nf * 0.18u' as='int((nf+2)/2) * W/nf * 0.18u'
+ pd='2*int((nf+1)/2) * (W/nf + 0.18u)' ps='2*int((nf+2)/2) * (W/nf + 0.18u)' nrd='0.18u / W' nrs='0.18u / W'
+ sa=0 sb=0 sd=0 m=1
XM1[80] Vout vg net3 net3 pfet_03v3 L=2u W=2u nf=1 ad='int((nf+1)/2) * W/nf * 0.18u' as='int((nf+2)/2) * W/nf * 0.18u'
+ pd='2*int((nf+1)/2) * (W/nf + 0.18u)' ps='2*int((nf+2)/2) * (W/nf + 0.18u)' nrd='0.18u / W' nrs='0.18u / W'
+ sa=0 sb=0 sd=0 m=1
XM1[81] Vout vg net3 net3 pfet_03v3 L=2u W=2u nf=1 ad='int((nf+1)/2) * W/nf * 0.18u' as='int((nf+2)/2) * W/nf * 0.18u'
+ pd='2*int((nf+1)/2) * (W/nf + 0.18u)' ps='2*int((nf+2)/2) * (W/nf + 0.18u)' nrd='0.18u / W' nrs='0.18u / W'
+ sa=0 sb=0 sd=0 m=1
XM1[82] Vout vg net3 net3 pfet_03v3 L=2u W=2u nf=1 ad='int((nf+1)/2) * W/nf * 0.18u' as='int((nf+2)/2) * W/nf * 0.18u'
+ pd='2*int((nf+1)/2) * (W/nf + 0.18u)' ps='2*int((nf+2)/2) * (W/nf + 0.18u)' nrd='0.18u / W' nrs='0.18u / W'
+ sa=0 sb=0 sd=0 m=1
XM1[83] Vout vg net3 net3 pfet_03v3 L=2u W=2u nf=1 ad='int((nf+1)/2) * W/nf * 0.18u' as='int((nf+2)/2) * W/nf * 0.18u'
+ pd='2*int((nf+1)/2) * (W/nf + 0.18u)' ps='2*int((nf+2)/2) * (W/nf + 0.18u)' nrd='0.18u / W' nrs='0.18u / W'
+ sa=0 sb=0 sd=0 m=1
XM1[84] Vout vg net3 net3 pfet_03v3 L=2u W=2u nf=1 ad='int((nf+1)/2) * W/nf * 0.18u' as='int((nf+2)/2) * W/nf * 0.18u'
+ pd='2*int((nf+1)/2) * (W/nf + 0.18u)' ps='2*int((nf+2)/2) * (W/nf + 0.18u)' nrd='0.18u / W' nrs='0.18u / W'
+ sa=0 sb=0 sd=0 m=1
XM1[85] Vout vg net3 net3 pfet_03v3 L=2u W=2u nf=1 ad='int((nf+1)/2) * W/nf * 0.18u' as='int((nf+2)/2) * W/nf * 0.18u'
+ pd='2*int((nf+1)/2) * (W/nf + 0.18u)' ps='2*int((nf+2)/2) * (W/nf + 0.18u)' nrd='0.18u / W' nrs='0.18u / W'
+ sa=0 sb=0 sd=0 m=1
XM1[86] Vout vg net3 net3 pfet_03v3 L=2u W=2u nf=1 ad='int((nf+1)/2) * W/nf * 0.18u' as='int((nf+2)/2) * W/nf * 0.18u'
+ pd='2*int((nf+1)/2) * (W/nf + 0.18u)' ps='2*int((nf+2)/2) * (W/nf + 0.18u)' nrd='0.18u / W' nrs='0.18u / W'
+ sa=0 sb=0 sd=0 m=1
XM1[87] Vout vg net3 net3 pfet_03v3 L=2u W=2u nf=1 ad='int((nf+1)/2) * W/nf * 0.18u' as='int((nf+2)/2) * W/nf * 0.18u'
+ pd='2*int((nf+1)/2) * (W/nf + 0.18u)' ps='2*int((nf+2)/2) * (W/nf + 0.18u)' nrd='0.18u / W' nrs='0.18u / W'
+ sa=0 sb=0 sd=0 m=1
XM1[88] Vout vg net3 net3 pfet_03v3 L=2u W=2u nf=1 ad='int((nf+1)/2) * W/nf * 0.18u' as='int((nf+2)/2) * W/nf * 0.18u'
+ pd='2*int((nf+1)/2) * (W/nf + 0.18u)' ps='2*int((nf+2)/2) * (W/nf + 0.18u)' nrd='0.18u / W' nrs='0.18u / W'
+ sa=0 sb=0 sd=0 m=1
XM1[89] Vout vg net3 net3 pfet_03v3 L=2u W=2u nf=1 ad='int((nf+1)/2) * W/nf * 0.18u' as='int((nf+2)/2) * W/nf * 0.18u'
+ pd='2*int((nf+1)/2) * (W/nf + 0.18u)' ps='2*int((nf+2)/2) * (W/nf + 0.18u)' nrd='0.18u / W' nrs='0.18u / W'
+ sa=0 sb=0 sd=0 m=1
XM1[90] Vout vg net3 net3 pfet_03v3 L=2u W=2u nf=1 ad='int((nf+1)/2) * W/nf * 0.18u' as='int((nf+2)/2) * W/nf * 0.18u'
+ pd='2*int((nf+1)/2) * (W/nf + 0.18u)' ps='2*int((nf+2)/2) * (W/nf + 0.18u)' nrd='0.18u / W' nrs='0.18u / W'
+ sa=0 sb=0 sd=0 m=1
XM1[91] Vout vg net3 net3 pfet_03v3 L=2u W=2u nf=1 ad='int((nf+1)/2) * W/nf * 0.18u' as='int((nf+2)/2) * W/nf * 0.18u'
+ pd='2*int((nf+1)/2) * (W/nf + 0.18u)' ps='2*int((nf+2)/2) * (W/nf + 0.18u)' nrd='0.18u / W' nrs='0.18u / W'
+ sa=0 sb=0 sd=0 m=1
XM1[92] Vout vg net3 net3 pfet_03v3 L=2u W=2u nf=1 ad='int((nf+1)/2) * W/nf * 0.18u' as='int((nf+2)/2) * W/nf * 0.18u'
+ pd='2*int((nf+1)/2) * (W/nf + 0.18u)' ps='2*int((nf+2)/2) * (W/nf + 0.18u)' nrd='0.18u / W' nrs='0.18u / W'
+ sa=0 sb=0 sd=0 m=1
XM1[93] Vout vg net3 net3 pfet_03v3 L=2u W=2u nf=1 ad='int((nf+1)/2) * W/nf * 0.18u' as='int((nf+2)/2) * W/nf * 0.18u'
+ pd='2*int((nf+1)/2) * (W/nf + 0.18u)' ps='2*int((nf+2)/2) * (W/nf + 0.18u)' nrd='0.18u / W' nrs='0.18u / W'
+ sa=0 sb=0 sd=0 m=1
XM1[94] Vout vg net3 net3 pfet_03v3 L=2u W=2u nf=1 ad='int((nf+1)/2) * W/nf * 0.18u' as='int((nf+2)/2) * W/nf * 0.18u'
+ pd='2*int((nf+1)/2) * (W/nf + 0.18u)' ps='2*int((nf+2)/2) * (W/nf + 0.18u)' nrd='0.18u / W' nrs='0.18u / W'
+ sa=0 sb=0 sd=0 m=1
XM1[95] Vout vg net3 net3 pfet_03v3 L=2u W=2u nf=1 ad='int((nf+1)/2) * W/nf * 0.18u' as='int((nf+2)/2) * W/nf * 0.18u'
+ pd='2*int((nf+1)/2) * (W/nf + 0.18u)' ps='2*int((nf+2)/2) * (W/nf + 0.18u)' nrd='0.18u / W' nrs='0.18u / W'
+ sa=0 sb=0 sd=0 m=1
XM1[96] Vout vg net3 net3 pfet_03v3 L=2u W=2u nf=1 ad='int((nf+1)/2) * W/nf * 0.18u' as='int((nf+2)/2) * W/nf * 0.18u'
+ pd='2*int((nf+1)/2) * (W/nf + 0.18u)' ps='2*int((nf+2)/2) * (W/nf + 0.18u)' nrd='0.18u / W' nrs='0.18u / W'
+ sa=0 sb=0 sd=0 m=1
XM1[97] Vout vg net3 net3 pfet_03v3 L=2u W=2u nf=1 ad='int((nf+1)/2) * W/nf * 0.18u' as='int((nf+2)/2) * W/nf * 0.18u'
+ pd='2*int((nf+1)/2) * (W/nf + 0.18u)' ps='2*int((nf+2)/2) * (W/nf + 0.18u)' nrd='0.18u / W' nrs='0.18u / W'
+ sa=0 sb=0 sd=0 m=1
XM1[98] Vout vg net3 net3 pfet_03v3 L=2u W=2u nf=1 ad='int((nf+1)/2) * W/nf * 0.18u' as='int((nf+2)/2) * W/nf * 0.18u'
+ pd='2*int((nf+1)/2) * (W/nf + 0.18u)' ps='2*int((nf+2)/2) * (W/nf + 0.18u)' nrd='0.18u / W' nrs='0.18u / W'
+ sa=0 sb=0 sd=0 m=1
XM1[99] Vout vg net3 net3 pfet_03v3 L=2u W=2u nf=1 ad='int((nf+1)/2) * W/nf * 0.18u' as='int((nf+2)/2) * W/nf * 0.18u'
+ pd='2*int((nf+1)/2) * (W/nf + 0.18u)' ps='2*int((nf+2)/2) * (W/nf + 0.18u)' nrd='0.18u / W' nrs='0.18u / W'
+ sa=0 sb=0 sd=0 m=1
XM1[100] Vout vg net3 net3 pfet_03v3 L=2u W=2u nf=1 ad='int((nf+1)/2) * W/nf * 0.18u' as='int((nf+2)/2) * W/nf * 0.18u'
+ pd='2*int((nf+1)/2) * (W/nf + 0.18u)' ps='2*int((nf+2)/2) * (W/nf + 0.18u)' nrd='0.18u / W' nrs='0.18u / W'
+ sa=0 sb=0 sd=0 m=1
XM1[101] Vout vg net3 net3 pfet_03v3 L=2u W=2u nf=1 ad='int((nf+1)/2) * W/nf * 0.18u' as='int((nf+2)/2) * W/nf * 0.18u'
+ pd='2*int((nf+1)/2) * (W/nf + 0.18u)' ps='2*int((nf+2)/2) * (W/nf + 0.18u)' nrd='0.18u / W' nrs='0.18u / W'
+ sa=0 sb=0 sd=0 m=1
XM1[102] Vout vg net3 net3 pfet_03v3 L=2u W=2u nf=1 ad='int((nf+1)/2) * W/nf * 0.18u' as='int((nf+2)/2) * W/nf * 0.18u'
+ pd='2*int((nf+1)/2) * (W/nf + 0.18u)' ps='2*int((nf+2)/2) * (W/nf + 0.18u)' nrd='0.18u / W' nrs='0.18u / W'
+ sa=0 sb=0 sd=0 m=1
XM1[103] Vout vg net3 net3 pfet_03v3 L=2u W=2u nf=1 ad='int((nf+1)/2) * W/nf * 0.18u' as='int((nf+2)/2) * W/nf * 0.18u'
+ pd='2*int((nf+1)/2) * (W/nf + 0.18u)' ps='2*int((nf+2)/2) * (W/nf + 0.18u)' nrd='0.18u / W' nrs='0.18u / W'
+ sa=0 sb=0 sd=0 m=1
XM1[104] Vout vg net3 net3 pfet_03v3 L=2u W=2u nf=1 ad='int((nf+1)/2) * W/nf * 0.18u' as='int((nf+2)/2) * W/nf * 0.18u'
+ pd='2*int((nf+1)/2) * (W/nf + 0.18u)' ps='2*int((nf+2)/2) * (W/nf + 0.18u)' nrd='0.18u / W' nrs='0.18u / W'
+ sa=0 sb=0 sd=0 m=1
XM1[105] Vout vg net3 net3 pfet_03v3 L=2u W=2u nf=1 ad='int((nf+1)/2) * W/nf * 0.18u' as='int((nf+2)/2) * W/nf * 0.18u'
+ pd='2*int((nf+1)/2) * (W/nf + 0.18u)' ps='2*int((nf+2)/2) * (W/nf + 0.18u)' nrd='0.18u / W' nrs='0.18u / W'
+ sa=0 sb=0 sd=0 m=1
XM1[106] Vout vg net3 net3 pfet_03v3 L=2u W=2u nf=1 ad='int((nf+1)/2) * W/nf * 0.18u' as='int((nf+2)/2) * W/nf * 0.18u'
+ pd='2*int((nf+1)/2) * (W/nf + 0.18u)' ps='2*int((nf+2)/2) * (W/nf + 0.18u)' nrd='0.18u / W' nrs='0.18u / W'
+ sa=0 sb=0 sd=0 m=1
XM1[107] Vout vg net3 net3 pfet_03v3 L=2u W=2u nf=1 ad='int((nf+1)/2) * W/nf * 0.18u' as='int((nf+2)/2) * W/nf * 0.18u'
+ pd='2*int((nf+1)/2) * (W/nf + 0.18u)' ps='2*int((nf+2)/2) * (W/nf + 0.18u)' nrd='0.18u / W' nrs='0.18u / W'
+ sa=0 sb=0 sd=0 m=1
XM1[108] Vout vg net3 net3 pfet_03v3 L=2u W=2u nf=1 ad='int((nf+1)/2) * W/nf * 0.18u' as='int((nf+2)/2) * W/nf * 0.18u'
+ pd='2*int((nf+1)/2) * (W/nf + 0.18u)' ps='2*int((nf+2)/2) * (W/nf + 0.18u)' nrd='0.18u / W' nrs='0.18u / W'
+ sa=0 sb=0 sd=0 m=1
XM1[109] Vout vg net3 net3 pfet_03v3 L=2u W=2u nf=1 ad='int((nf+1)/2) * W/nf * 0.18u' as='int((nf+2)/2) * W/nf * 0.18u'
+ pd='2*int((nf+1)/2) * (W/nf + 0.18u)' ps='2*int((nf+2)/2) * (W/nf + 0.18u)' nrd='0.18u / W' nrs='0.18u / W'
+ sa=0 sb=0 sd=0 m=1
XM1[110] Vout vg net3 net3 pfet_03v3 L=2u W=2u nf=1 ad='int((nf+1)/2) * W/nf * 0.18u' as='int((nf+2)/2) * W/nf * 0.18u'
+ pd='2*int((nf+1)/2) * (W/nf + 0.18u)' ps='2*int((nf+2)/2) * (W/nf + 0.18u)' nrd='0.18u / W' nrs='0.18u / W'
+ sa=0 sb=0 sd=0 m=1
Vmeas1 net2 vg 0
.save i(vmeas1)
Iload net5 GND pulse(5m 0 5u 1u 1u 10u 100u)
Vmeas3 AVDD net3 0
.save i(vmeas3)
Vmeas4 Vout net5 0
.save i(vmeas4)
C2 Vout vg 2p m=1
C1 Vout GND 1p m=1
x1 vref_off Vin net2 net4 AVDD GND FoldedCascode
VDD1 Vin GND 1.3626
VDD2 net1 GND pulse(0 0.3 40u 200n 200n 10u 100u)
XR2 vref_off Vout GND ppolyf_u_1k r_width=1e-6 r_length=8e-6 m=1
XR3 net6 vref_off GND ppolyf_u_1k r_width=1.2e-6 r_length=46.4e-6 m=1
**** begin user architecture code

.include $::180MCU_MODELS/design.ngspice
.lib $::180MCU_MODELS/sm141064.ngspice typical
.lib $::180MCU_MODELS/sm141064.ngspice res_typical
*.lib $::180MCU_MODELS/sm141064.ngspice res_statistical
*.param sw_stat_mismatch=1
*.param sw_stat_global=1



.option gmin=1e-15
.option klu

.control
save all
set temp = 27


tran 20n 60u
remzerovec
write TB_LDO_tran.raw
set appendwrite

op
remzerovec
write TB_LDO_tran.raw
set appendwrite




.endc
.save all


**** end user architecture code
**.ends
.GLOBAL GND
.end
